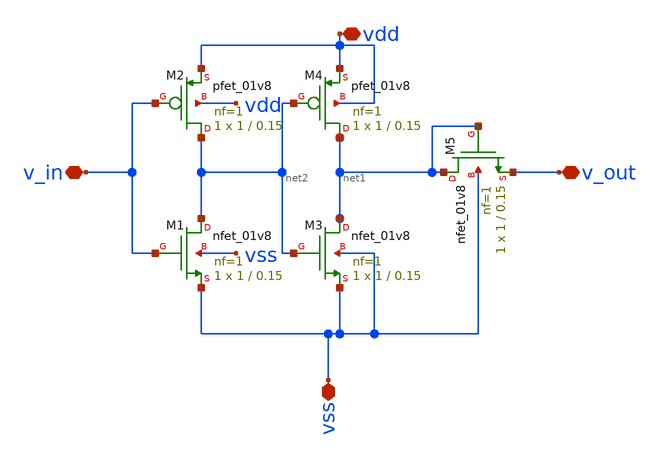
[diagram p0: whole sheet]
** sch_path: Synapse/syn_rep.sch
**.subckt syn_rep v_in vdd vss v_out
*.iopin v_in
*.iopin vdd
*.iopin vss
*.iopin v_out
XM1 net2 v_in vss vss sky130_fd_pr__nfet_01v8 L=0.15 W=1 nf=1 ad='int((nf+1)/2) * W/nf * 0.29' as='int((nf+2)/2) * W/nf * 0.29'
+ pd='2*int((nf+1)/2) * (W/nf + 0.29)' ps='2*int((nf+2)/2) * (W/nf + 0.29)' nrd='0.29 / W' nrs='0.29 / W'
+ sa=0 sb=0 sd=0 mult=1 m=1
XM2 net2 v_in vdd vdd sky130_fd_pr__pfet_01v8 L=0.15 W=1 nf=1 ad='int((nf+1)/2) * W/nf * 0.29' as='int((nf+2)/2) * W/nf * 0.29'
+ pd='2*int((nf+1)/2) * (W/nf + 0.29)' ps='2*int((nf+2)/2) * (W/nf + 0.29)' nrd='0.29 / W' nrs='0.29 / W'
+ sa=0 sb=0 sd=0 mult=1 m=1
XM3 net1 net2 vss vss sky130_fd_pr__nfet_01v8 L=0.15 W=1 nf=1 ad='int((nf+1)/2) * W/nf * 0.29' as='int((nf+2)/2) * W/nf * 0.29'
+ pd='2*int((nf+1)/2) * (W/nf + 0.29)' ps='2*int((nf+2)/2) * (W/nf + 0.29)' nrd='0.29 / W' nrs='0.29 / W'
+ sa=0 sb=0 sd=0 mult=1 m=1
XM4 net1 net2 vdd vdd sky130_fd_pr__pfet_01v8 L=0.15 W=1 nf=1 ad='int((nf+1)/2) * W/nf * 0.29' as='int((nf+2)/2) * W/nf * 0.29'
+ pd='2*int((nf+1)/2) * (W/nf + 0.29)' ps='2*int((nf+2)/2) * (W/nf + 0.29)' nrd='0.29 / W' nrs='0.29 / W'
+ sa=0 sb=0 sd=0 mult=1 m=1
XM5 net1 net1 v_out vss sky130_fd_pr__nfet_01v8 L=0.15 W=1 nf=1 ad='int((nf+1)/2) * W/nf * 0.29' as='int((nf+2)/2) * W/nf * 0.29'
+ pd='2*int((nf+1)/2) * (W/nf + 0.29)' ps='2*int((nf+2)/2) * (W/nf + 0.29)' nrd='0.29 / W' nrs='0.29 / W'
+ sa=0 sb=0 sd=0 mult=1 m=1
**.ends
.end
